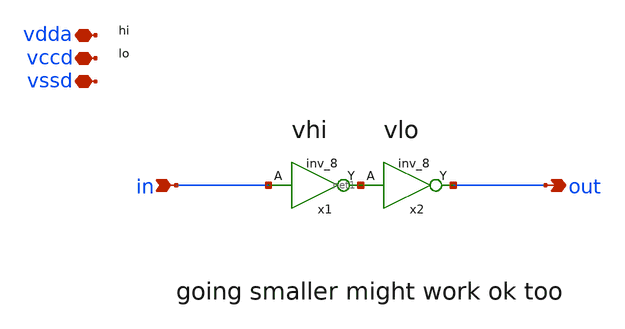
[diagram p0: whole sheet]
** sch_path: xschem/level_shifter/level_down_shifter.sch
**.subckt level_down_shifter in vssd vdda out vccd
*.ipin in
*.iopin vssd
*.iopin vdda
*.opin out
*.iopin vccd
x1 in vssd vssd vdda vdda net1 sky130_fd_sc_hd__inv_8
x2 net1 vssd vssd vccd vccd out sky130_fd_sc_hd__inv_8
**.ends
.end
